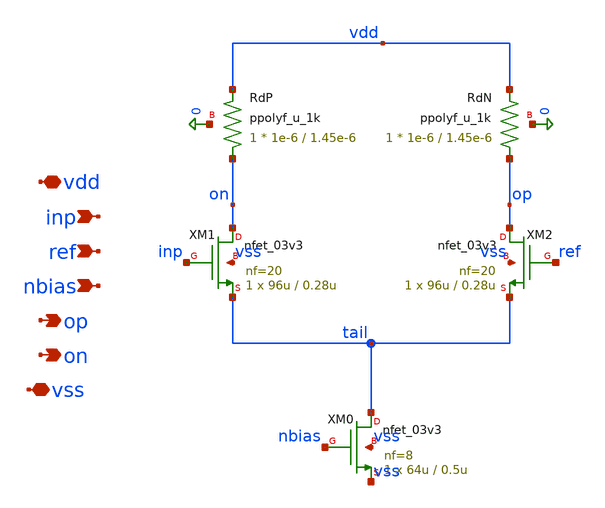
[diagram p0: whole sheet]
** sch_path: blocks/adc/comp-array/preamp.sch
**.subckt preamp vdd inp ref nbias op on vss
*.iopin vdd
*.ipin inp
*.ipin ref
*.ipin nbias
*.opin op
*.opin on
*.iopin vss
XM0 tail nbias vss vss nfet_03v3 L=0.5u W=64u nf=8 ad='int((nf+1)/2) * W/nf * 0.18u' as='int((nf+2)/2) * W/nf * 0.18u'
+ pd='2*int((nf+1)/2) * (W/nf + 0.18u)' ps='2*int((nf+2)/2) * (W/nf + 0.18u)' nrd='0.18u / W' nrs='0.18u / W'
+ sa=0 sb=0 sd=0 m=1
XM1 on inp tail vss nfet_03v3 L=0.28u W=96u nf=20 ad='int((nf+1)/2) * W/nf * 0.18u' as='int((nf+2)/2) * W/nf * 0.18u'
+ pd='2*int((nf+1)/2) * (W/nf + 0.18u)' ps='2*int((nf+2)/2) * (W/nf + 0.18u)' nrd='0.18u / W' nrs='0.18u / W'
+ sa=0 sb=0 sd=0 m=1
XM2 op ref tail vss nfet_03v3 L=0.28u W=96u nf=20 ad='int((nf+1)/2) * W/nf * 0.18u' as='int((nf+2)/2) * W/nf * 0.18u'
+ pd='2*int((nf+1)/2) * (W/nf + 0.18u)' ps='2*int((nf+2)/2) * (W/nf + 0.18u)' nrd='0.18u / W' nrs='0.18u / W'
+ sa=0 sb=0 sd=0 m=1
XRdP on vdd 0 ppolyf_u_1k r_width=1e-6 r_length=1.45e-6 m=1
XRdN op vdd 0 ppolyf_u_1k r_width=1e-6 r_length=1.45e-6 m=1
**.ends
.end
